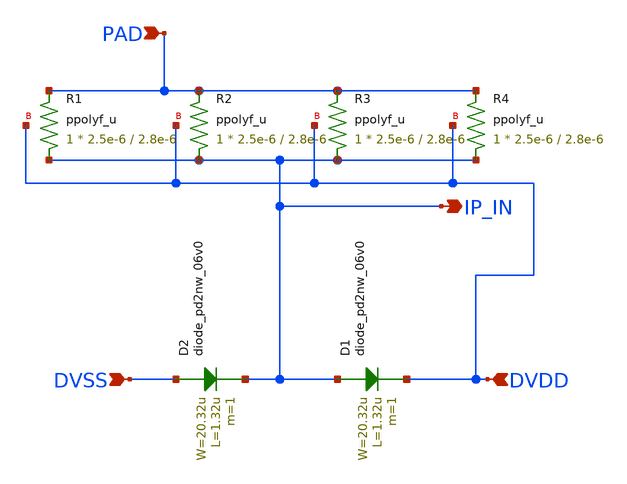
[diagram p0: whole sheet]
** sch_path: gf180mcu_fd_io__bi_24t/comp018green_esd_cdm.sch
**.subckt comp018green_esd_cdm PAD DVDD DVSS IP_IN
*.ipin PAD
*.ipin DVDD
*.ipin DVSS
*.opin IP_IN
XR1 IP_IN PAD DVDD ppolyf_u r_width=2.5e-6 r_length=2.8e-6 m=1
XR2 IP_IN PAD DVDD ppolyf_u r_width=2.5e-6 r_length=2.8e-6 m=1
XR3 IP_IN PAD DVDD ppolyf_u r_width=2.5e-6 r_length=2.8e-6 m=1
XR4 IP_IN PAD DVDD ppolyf_u r_width=2.5e-6 r_length=2.8e-6 m=1
D1 IP_IN DVDD diode_pd2nw_06v0 area='20.32u * 1.32u ' pj='2*20.32u + 2*1.32u ' m=1
D2 DVSS IP_IN diode_pd2nw_06v0 area='20.32u * 1.32u ' pj='2*20.32u + 2*1.32u ' m=1
**.ends
.end
